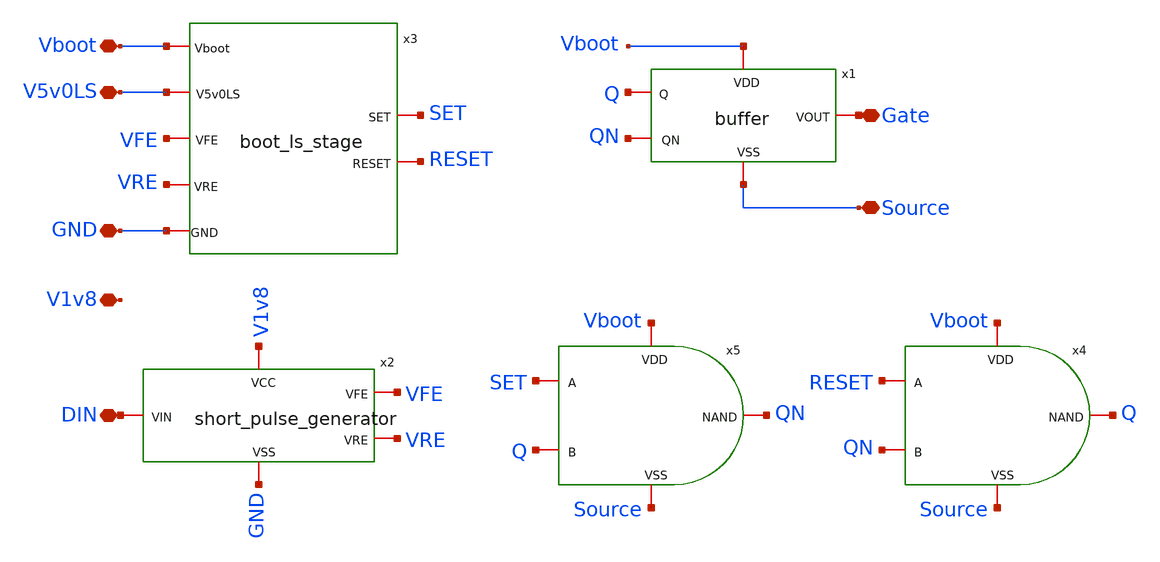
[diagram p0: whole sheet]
** sch_path: xschem/driver_bootstrap.sch
**.subckt driver_bootstrap Gate V5v0LS DIN V1v8 GND Source Vboot
*.iopin Gate
*.iopin V5v0LS
*.iopin DIN
*.iopin V1v8
*.iopin GND
*.iopin Source
*.iopin Vboot
x3 Vboot V5v0LS SET RESET GND VFE VRE boot_ls_stage
x2 V1v8 GND VFE DIN VRE short_pulse_generator
x1 Vboot Gate Source QN Q buffer
x4 Vboot RESET QN Q Source nand_5v
x5 Vboot SET Q QN Source nand_5v
**.ends

* expanding   symbol:  /foss/designs/Open3LFCC_V2_GD12V/xschem/boot_ls_stage.sym # of pins=7
** sym_path: xschem/boot_ls_stage.sym
** sch_path: xschem/boot_ls_stage.sch
.subckt boot_ls_stage Vboot V5v0LS SET RESET GND VFE VRE
*.iopin V5v0LS
*.iopin GND
*.iopin Vboot
*.iopin VFE
*.iopin VRE
*.iopin SET
*.iopin RESET
XM7 net1 RESET Vboot Vboot sky130_fd_pr__pfet_g5v0d10v5 L=0.5 W=1 nf=1 ad='int((nf+1)/2) * W/nf * 0.29'
+ as='int((nf+2)/2) * W/nf * 0.29' pd='2*int((nf+1)/2) * (W/nf + 0.29)' ps='2*int((nf+2)/2) * (W/nf + 0.29)'
+ nrd='0.29 / W' nrs='0.29 / W' sa=0 sb=0 sd=0 mult=1 m=1
XM8 SET SET net1 net1 sky130_fd_pr__pfet_g5v0d10v5 L=0.5 W=1 nf=1 ad='int((nf+1)/2) * W/nf * 0.29' as='int((nf+2)/2) * W/nf * 0.29'
+ pd='2*int((nf+1)/2) * (W/nf + 0.29)' ps='2*int((nf+2)/2) * (W/nf + 0.29)' nrd='0.29 / W' nrs='0.29 / W'
+ sa=0 sb=0 sd=0 mult=1 m=1
XM4 RESET SET Vboot Vboot sky130_fd_pr__pfet_g5v0d10v5 L=1 W=5 nf=1 ad='int((nf+1)/2) * W/nf * 0.29'
+ as='int((nf+2)/2) * W/nf * 0.29' pd='2*int((nf+1)/2) * (W/nf + 0.29)' ps='2*int((nf+2)/2) * (W/nf + 0.29)'
+ nrd='0.29 / W' nrs='0.29 / W' sa=0 sb=0 sd=0 mult=1 m=1
XM3 SET SET Vboot Vboot sky130_fd_pr__pfet_g5v0d10v5 L=1 W=0.5 nf=1 ad='int((nf+1)/2) * W/nf * 0.29'
+ as='int((nf+2)/2) * W/nf * 0.29' pd='2*int((nf+1)/2) * (W/nf + 0.29)' ps='2*int((nf+2)/2) * (W/nf + 0.29)'
+ nrd='0.29 / W' nrs='0.29 / W' sa=0 sb=0 sd=0 mult=1 m=1
XM9 net3 SET Vboot Vboot sky130_fd_pr__pfet_g5v0d10v5 L=0.5 W=1 nf=1 ad='int((nf+1)/2) * W/nf * 0.29'
+ as='int((nf+2)/2) * W/nf * 0.29' pd='2*int((nf+1)/2) * (W/nf + 0.29)' ps='2*int((nf+2)/2) * (W/nf + 0.29)'
+ nrd='0.29 / W' nrs='0.29 / W' sa=0 sb=0 sd=0 mult=1 m=1
XM10 RESET RESET net3 net3 sky130_fd_pr__pfet_g5v0d10v5 L=0.5 W=1 nf=1 ad='int((nf+1)/2) * W/nf * 0.29'
+ as='int((nf+2)/2) * W/nf * 0.29' pd='2*int((nf+1)/2) * (W/nf + 0.29)' ps='2*int((nf+2)/2) * (W/nf + 0.29)'
+ nrd='0.29 / W' nrs='0.29 / W' sa=0 sb=0 sd=0 mult=1 m=1
XM5 SET RESET Vboot Vboot sky130_fd_pr__pfet_g5v0d10v5 L=1 W=5 nf=1 ad='int((nf+1)/2) * W/nf * 0.29'
+ as='int((nf+2)/2) * W/nf * 0.29' pd='2*int((nf+1)/2) * (W/nf + 0.29)' ps='2*int((nf+2)/2) * (W/nf + 0.29)'
+ nrd='0.29 / W' nrs='0.29 / W' sa=0 sb=0 sd=0 mult=1 m=1
XM6 RESET RESET Vboot Vboot sky130_fd_pr__pfet_g5v0d10v5 L=1 W=0.5 nf=1 ad='int((nf+1)/2) * W/nf * 0.29'
+ as='int((nf+2)/2) * W/nf * 0.29' pd='2*int((nf+1)/2) * (W/nf + 0.29)' ps='2*int((nf+2)/2) * (W/nf + 0.29)'
+ nrd='0.29 / W' nrs='0.29 / W' sa=0 sb=0 sd=0 mult=1 m=1
I0 V5v0LS net4 30u
XM11 net4 net4 GND GND sky130_fd_pr__nfet_g5v0d10v5 L=2 W=4 nf=1 ad='int((nf+1)/2) * W/nf * 0.29' as='int((nf+2)/2) * W/nf * 0.29'
+ pd='2*int((nf+1)/2) * (W/nf + 0.29)' ps='2*int((nf+2)/2) * (W/nf + 0.29)' nrd='0.29 / W' nrs='0.29 / W'
+ sa=0 sb=0 sd=0 mult=1 m=1
XM12 net2 net4 GND GND sky130_fd_pr__nfet_g5v0d10v5 L=2 W=8 nf=1 ad='int((nf+1)/2) * W/nf * 0.29' as='int((nf+2)/2) * W/nf * 0.29'
+ pd='2*int((nf+1)/2) * (W/nf + 0.29)' ps='2*int((nf+2)/2) * (W/nf + 0.29)' nrd='0.29 / W' nrs='0.29 / W'
+ sa=0 sb=0 sd=0 mult=1 m=1
XM1 SET VRE net2 net2 sky130_fd_pr__nfet_g5v0d10v5 L=0.5 W=6 nf=1 ad='int((nf+1)/2) * W/nf * 0.29' as='int((nf+2)/2) * W/nf * 0.29'
+ pd='2*int((nf+1)/2) * (W/nf + 0.29)' ps='2*int((nf+2)/2) * (W/nf + 0.29)' nrd='0.29 / W' nrs='0.29 / W'
+ sa=0 sb=0 sd=0 mult=1 m=1
XM2 RESET VFE net2 net2 sky130_fd_pr__nfet_g5v0d10v5 L=0.5 W=6 nf=1 ad='int((nf+1)/2) * W/nf * 0.29'
+ as='int((nf+2)/2) * W/nf * 0.29' pd='2*int((nf+1)/2) * (W/nf + 0.29)' ps='2*int((nf+2)/2) * (W/nf + 0.29)'
+ nrd='0.29 / W' nrs='0.29 / W' sa=0 sb=0 sd=0 mult=1 m=1
.ends


* expanding   symbol:  /foss/designs/Open3LFCC_V2_GD12V/xschem/short_pulse_generator.sym # of pins=5
** sym_path: xschem/short_pulse_generator.sym
** sch_path: xschem/short_pulse_generator.sch
.subckt short_pulse_generator VCC VSS VFE VIN VRE
*.iopin VIN
*.iopin VFE
*.iopin VRE
*.iopin VCC
*.iopin VSS
x3 net3 VSS VSS VCC VCC predly sky130_fd_sc_hd__inv_1
x4 predly VSS VSS VCC VCC net2 sky130_fd_sc_hd__inv_1
x5 dly8 VSS VSS VCC VCC net1 sky130_fd_sc_hd__inv_1
x6 VIN VSS VSS VCC VCC net3 sky130_fd_sc_hd__inv_2
x7 predly VSS VSS VCC VCC V_gatein sky130_fd_sc_hd__inv_8
x8 net2 dly8 VSS VSS VCC VCC VFE sky130_fd_sc_hd__and2_2
x9 net1 predly VSS VSS VCC VCC VRE sky130_fd_sc_hd__and2_2
x2 dly7 VSS VSS VCC VCC dly8 sky130_fd_sc_hd__inv_1
x10[0] V_gatein VSS VSS VCC VCC n2 sky130_fd_sc_hd__clkdlybuf4s50_2
x10[1] n2 VSS VSS VCC VCC n3 sky130_fd_sc_hd__clkdlybuf4s50_2
x10[2] n3 VSS VSS VCC VCC n4 sky130_fd_sc_hd__clkdlybuf4s50_2
x10[3] n4 VSS VSS VCC VCC n5 sky130_fd_sc_hd__clkdlybuf4s50_2
x10[4] n5 VSS VSS VCC VCC n6 sky130_fd_sc_hd__clkdlybuf4s50_2
x10[5] n6 VSS VSS VCC VCC n7 sky130_fd_sc_hd__clkdlybuf4s50_2
x10[6] n7 VSS VSS VCC VCC n8 sky130_fd_sc_hd__clkdlybuf4s50_2
x10[7] n8 VSS VSS VCC VCC n9 sky130_fd_sc_hd__clkdlybuf4s50_2
x10[8] n9 VSS VSS VCC VCC n10 sky130_fd_sc_hd__clkdlybuf4s50_2
x10[9] n10 VSS VSS VCC VCC n11 sky130_fd_sc_hd__clkdlybuf4s50_2
x10[10] n11 VSS VSS VCC VCC n12 sky130_fd_sc_hd__clkdlybuf4s50_2
x10[11] n12 VSS VSS VCC VCC n13 sky130_fd_sc_hd__clkdlybuf4s50_2
x10[12] n13 VSS VSS VCC VCC n14 sky130_fd_sc_hd__clkdlybuf4s50_2
x10[13] n14 VSS VSS VCC VCC n15 sky130_fd_sc_hd__clkdlybuf4s50_2
x10[14] n15 VSS VSS VCC VCC n16 sky130_fd_sc_hd__clkdlybuf4s50_2
x10[15] n16 VSS VSS VCC VCC n17 sky130_fd_sc_hd__clkdlybuf4s50_2
x10[16] n17 VSS VSS VCC VCC n18 sky130_fd_sc_hd__clkdlybuf4s50_2
x10[17] n18 VSS VSS VCC VCC n19 sky130_fd_sc_hd__clkdlybuf4s50_2
x10[18] n19 VSS VSS VCC VCC n20 sky130_fd_sc_hd__clkdlybuf4s50_2
x10[19] n20 VSS VSS VCC VCC n21 sky130_fd_sc_hd__clkdlybuf4s50_2
x10[20] n21 VSS VSS VCC VCC n22 sky130_fd_sc_hd__clkdlybuf4s50_2
x10[21] n22 VSS VSS VCC VCC n23 sky130_fd_sc_hd__clkdlybuf4s50_2
x10[22] n23 VSS VSS VCC VCC n24 sky130_fd_sc_hd__clkdlybuf4s50_2
x10[23] n24 VSS VSS VCC VCC n25 sky130_fd_sc_hd__clkdlybuf4s50_2
x10[24] n25 VSS VSS VCC VCC n26 sky130_fd_sc_hd__clkdlybuf4s50_2
x10[25] n26 VSS VSS VCC VCC n27 sky130_fd_sc_hd__clkdlybuf4s50_2
x10[26] n27 VSS VSS VCC VCC n28 sky130_fd_sc_hd__clkdlybuf4s50_2
x10[27] n28 VSS VSS VCC VCC n29 sky130_fd_sc_hd__clkdlybuf4s50_2
x10[28] n29 VSS VSS VCC VCC n30 sky130_fd_sc_hd__clkdlybuf4s50_2
x10[29] n30 VSS VSS VCC VCC n31 sky130_fd_sc_hd__clkdlybuf4s50_2
x10[30] n31 VSS VSS VCC VCC n32 sky130_fd_sc_hd__clkdlybuf4s50_2
x10[31] n32 VSS VSS VCC VCC n33 sky130_fd_sc_hd__clkdlybuf4s50_2
x10[32] n33 VSS VSS VCC VCC n34 sky130_fd_sc_hd__clkdlybuf4s50_2
x10[33] n34 VSS VSS VCC VCC n35 sky130_fd_sc_hd__clkdlybuf4s50_2
x10[34] n35 VSS VSS VCC VCC n36 sky130_fd_sc_hd__clkdlybuf4s50_2
x10[35] n36 VSS VSS VCC VCC dly7 sky130_fd_sc_hd__clkdlybuf4s50_2
**** begin user architecture code


*.lib /foss/pdks/sky130A/libs.tech/ngspice/sky130.lib.spice TT
.include /foss/pdks/sky130A/libs.ref/sky130_fd_sc_hd/spice/sky130_fd_sc_hd.spice


**** end user architecture code
.ends


* expanding   symbol:  /foss/designs/Open3LFCC_V2_GD12V/xschem/buffer.sym # of pins=5
** sym_path: xschem/buffer.sym
** sch_path: xschem/buffer.sch
.subckt buffer VDD VOUT VSS QN Q
*.iopin VDD
*.iopin VSS
*.iopin Q
*.iopin QN
*.iopin VOUT
XM15 net2 net1 VDD VDD sky130_fd_pr__pfet_g5v0d10v5 L=0.5 W=3 nf=1 ad='int((nf+1)/2) * W/nf * 0.29' as='int((nf+2)/2) * W/nf * 0.29'
+ pd='2*int((nf+1)/2) * (W/nf + 0.29)' ps='2*int((nf+2)/2) * (W/nf + 0.29)' nrd='0.29 / W' nrs='0.29 / W'
+ sa=0 sb=0 sd=0 mult=1 m=1
XM13 net1 net2 VDD VDD sky130_fd_pr__pfet_g5v0d10v5 L=0.5 W=1 nf=1 ad='int((nf+1)/2) * W/nf * 0.29' as='int((nf+2)/2) * W/nf * 0.29'
+ pd='2*int((nf+1)/2) * (W/nf + 0.29)' ps='2*int((nf+2)/2) * (W/nf + 0.29)' nrd='0.29 / W' nrs='0.29 / W'
+ sa=0 sb=0 sd=0 mult=1 m=1
XM17 VOUT net2 VDD VDD sky130_fd_pr__pfet_g5v0d10v5 L=0.5 W=10.84 nf=1 ad='int((nf+1)/2) * W/nf * 0.29'
+ as='int((nf+2)/2) * W/nf * 0.29' pd='2*int((nf+1)/2) * (W/nf + 0.29)' ps='2*int((nf+2)/2) * (W/nf + 0.29)'
+ nrd='0.29 / W' nrs='0.29 / W' sa=0 sb=0 sd=0 mult=18 m=18
XM14 net1 Q VSS VSS sky130_fd_pr__nfet_g5v0d10v5 L=0.5 W=3 nf=1 ad='int((nf+1)/2) * W/nf * 0.29' as='int((nf+2)/2) * W/nf * 0.29'
+ pd='2*int((nf+1)/2) * (W/nf + 0.29)' ps='2*int((nf+2)/2) * (W/nf + 0.29)' nrd='0.29 / W' nrs='0.29 / W'
+ sa=0 sb=0 sd=0 mult=1 m=1
XM16 net2 QN VSS VSS sky130_fd_pr__nfet_g5v0d10v5 L=0.5 W=3 nf=1 ad='int((nf+1)/2) * W/nf * 0.29' as='int((nf+2)/2) * W/nf * 0.29'
+ pd='2*int((nf+1)/2) * (W/nf + 0.29)' ps='2*int((nf+2)/2) * (W/nf + 0.29)' nrd='0.29 / W' nrs='0.29 / W'
+ sa=0 sb=0 sd=0 mult=1 m=1
XM18 VOUT net2 VSS VSS sky130_fd_pr__nfet_g5v0d10v5 L=0.5 W=4 nf=1 ad='int((nf+1)/2) * W/nf * 0.29' as='int((nf+2)/2) * W/nf * 0.29'
+ pd='2*int((nf+1)/2) * (W/nf + 0.29)' ps='2*int((nf+2)/2) * (W/nf + 0.29)' nrd='0.29 / W' nrs='0.29 / W'
+ sa=0 sb=0 sd=0 mult=18 m=18
.ends


* expanding   symbol:  /foss/designs/Open3LFCC_V2_GD12V/xschem/nand_5v.sym # of pins=5
** sym_path: xschem/nand_5v.sym
** sch_path: xschem/nand_5v.sch
.subckt nand_5v VDD A B NAND VSS
*.iopin VSS
*.iopin VDD
*.iopin A
*.iopin B
*.iopin NAND
XM25 net1 B VSS VSS sky130_fd_pr__nfet_g5v0d10v5 L=3 W=0.5 nf=1 ad='int((nf+1)/2) * W/nf * 0.29' as='int((nf+2)/2) * W/nf * 0.29'
+ pd='2*int((nf+1)/2) * (W/nf + 0.29)' ps='2*int((nf+2)/2) * (W/nf + 0.29)' nrd='0.29 / W' nrs='0.29 / W'
+ sa=0 sb=0 sd=0 mult=10 m=10
XM26 NAND A net1 VSS sky130_fd_pr__nfet_g5v0d10v5 L=3 W=0.5 nf=1 ad='int((nf+1)/2) * W/nf * 0.29' as='int((nf+2)/2) * W/nf * 0.29'
+ pd='2*int((nf+1)/2) * (W/nf + 0.29)' ps='2*int((nf+2)/2) * (W/nf + 0.29)' nrd='0.29 / W' nrs='0.29 / W'
+ sa=0 sb=0 sd=0 mult=10 m=10
XM27 NAND A VDD VDD sky130_fd_pr__pfet_g5v0d10v5 L=3 W=0.5 nf=1 ad='int((nf+1)/2) * W/nf * 0.29' as='int((nf+2)/2) * W/nf * 0.29'
+ pd='2*int((nf+1)/2) * (W/nf + 0.29)' ps='2*int((nf+2)/2) * (W/nf + 0.29)' nrd='0.29 / W' nrs='0.29 / W'
+ sa=0 sb=0 sd=0 mult=10 m=10
XM28 NAND B VDD VDD sky130_fd_pr__pfet_g5v0d10v5 L=3 W=0.5 nf=1 ad='int((nf+1)/2) * W/nf * 0.29' as='int((nf+2)/2) * W/nf * 0.29'
+ pd='2*int((nf+1)/2) * (W/nf + 0.29)' ps='2*int((nf+2)/2) * (W/nf + 0.29)' nrd='0.29 / W' nrs='0.29 / W'
+ sa=0 sb=0 sd=0 mult=10 m=10
.ends

.end
